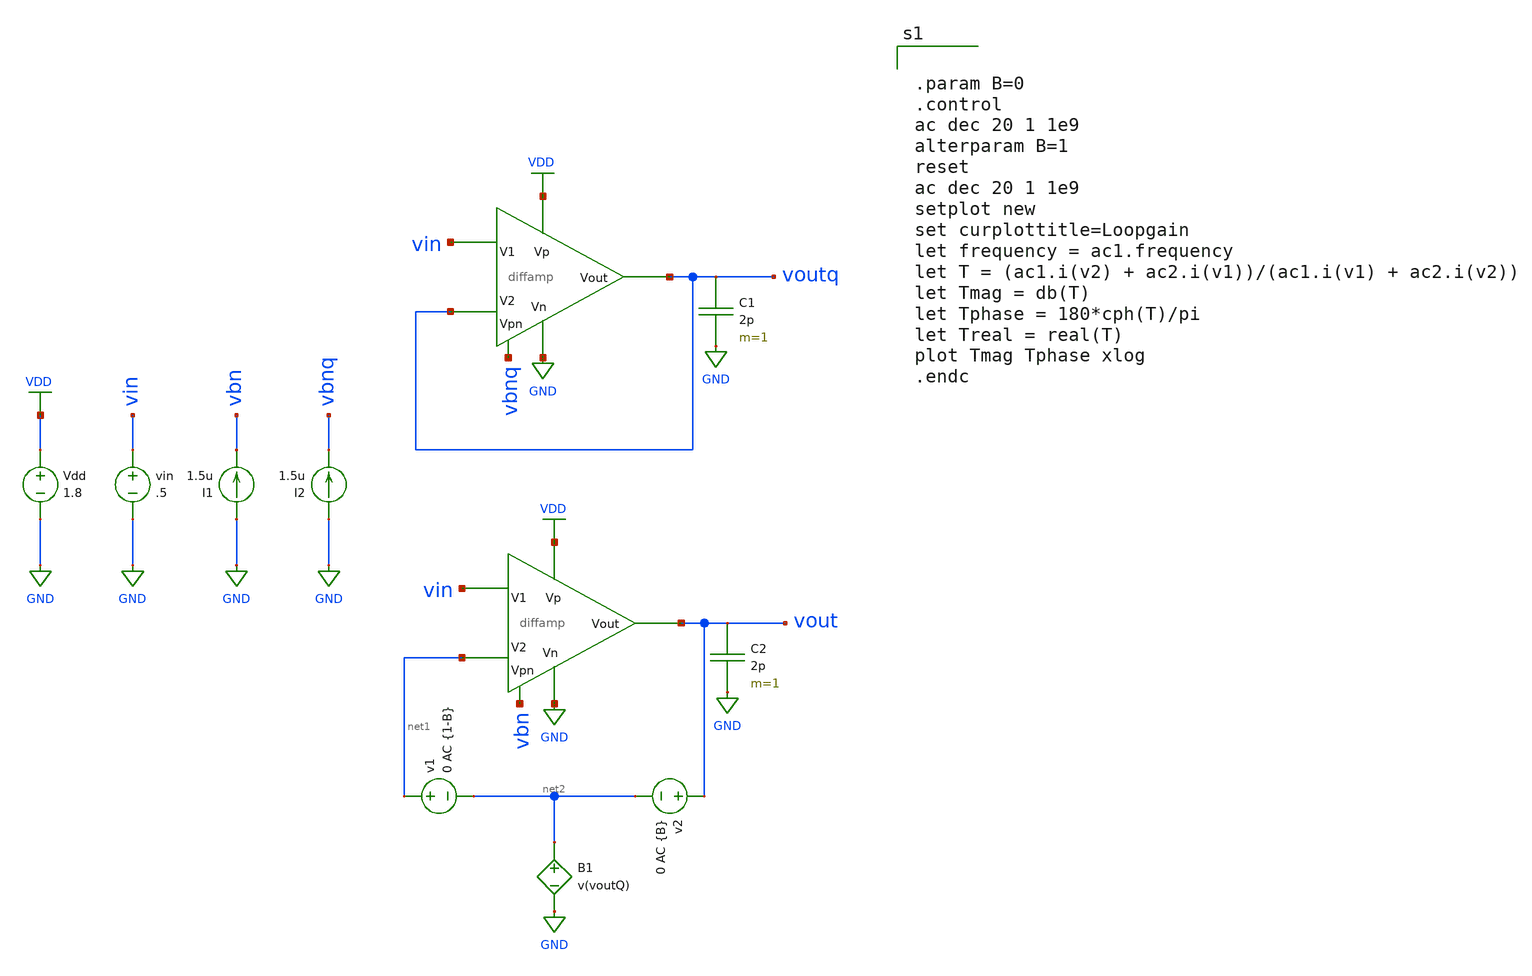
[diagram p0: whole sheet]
** sch_path: mini_proj_3/schematic/diff_2c.sch
**.subckt diff_2c
Vdd VDD GND 1.8
vin vin GND .5
I1 GND vbn 1.5u
C1 voutq GND 2p m=1
C2 vout GND 2p m=1
I2 GND vbnq 1.5u
v1 net1 net2 0 AC {1-B}
v2 vout net2 0 AC {B}
B1 net2 GND V=v(voutQ)
X1 vbnq VDD GND vin voutq voutq diffamp
X2 vbn VDD GND vin net1 vout diffamp
**** begin user architecture code

.option wnflag=1
.lib ~/skywater/skywater-pdk/libraries/sky130_fd_pr_ngspice/latest/models/sky130.lib.spice tt



.param B=0
.control
ac dec 20 1 1e9
alterparam B=1
reset
ac dec 20 1 1e9
setplot new
set curplottitle=Loopgain
let frequency = ac1.frequency
let T = (ac1.i(v2) + ac2.i(v1))/(ac1.i(v1) + ac2.i(v2))
let Tmag = db(T)
let Tphase = 180*cph(T)/pi
let Treal = real(T)
plot Tmag Tphase xlog
.endc

**** end user architecture code
**.ends
.GLOBAL VDD
.GLOBAL GND
.end
